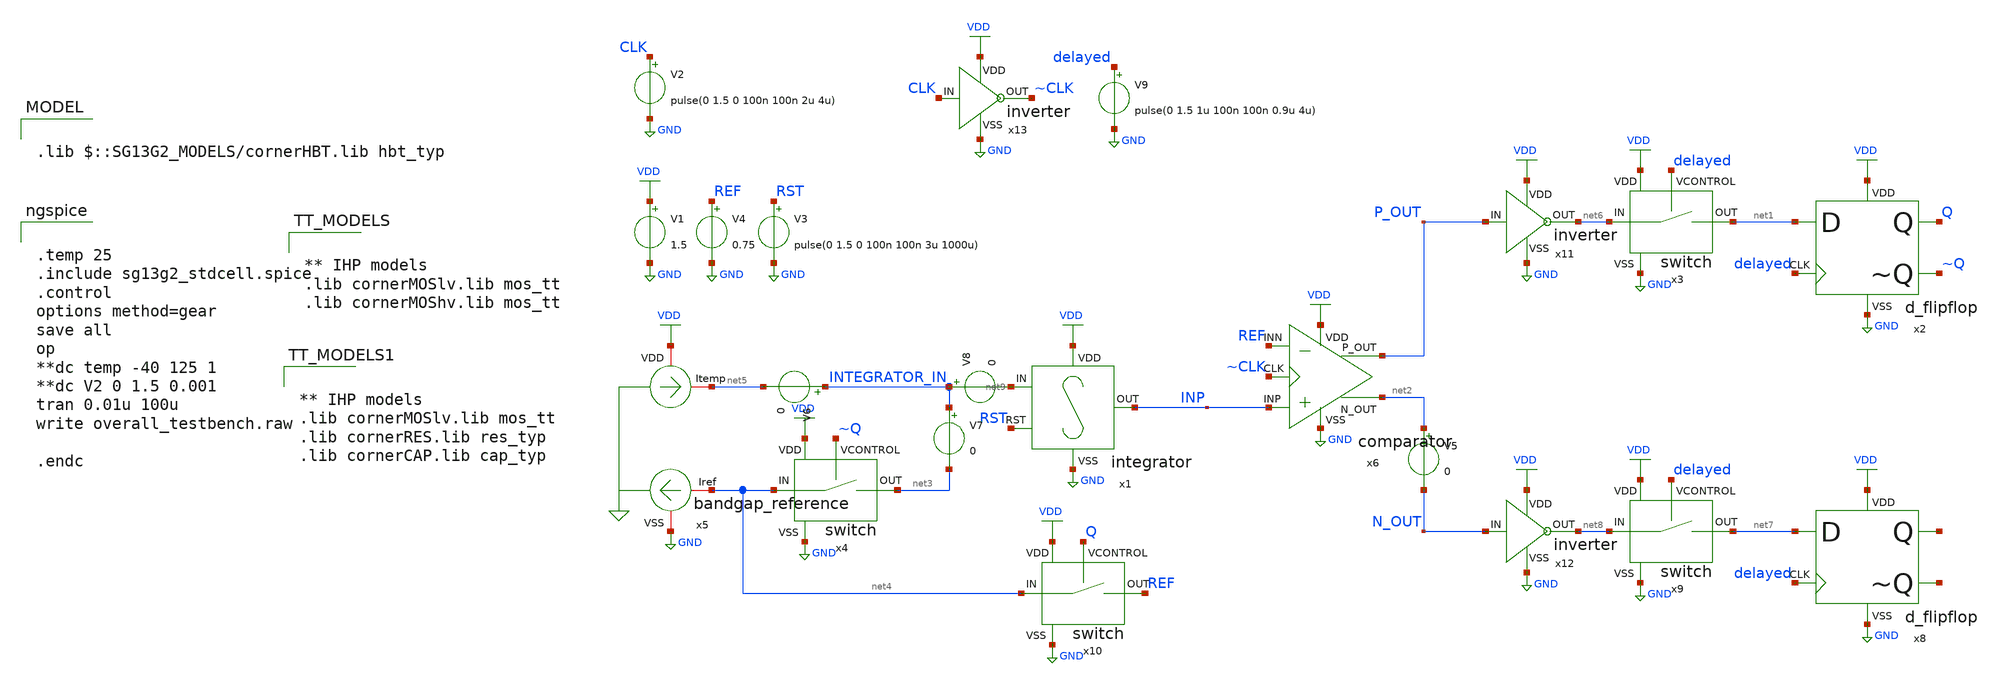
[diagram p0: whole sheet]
** sch_path: 10_xschem/overall_circuit_testbench.sch
**.subckt overall_circuit_testbench
x1 INP net9 VDD GND RST integrator
x4 net3 net4 VDD ~Q GND switch
V1 VDD GND 1.5
V3 RST GND pulse(0 1.5 0 100n 100n 3u 1000u)
x6 VDD P_OUT net2 ~CLK REF INP GND comparator
V4 REF GND 0.75
x2 Q ~Q net1 VDD GND delayed d_flipflop
x3 net1 net6 VDD delayed GND switch
x10 REF net4 VDD Q GND switch
V5 net2 N_OUT 0
V6 INTEGRATOR_IN net5 0
V7 INTEGRATOR_IN net3 0
x11 VDD P_OUT net6 GND inverter
x12 VDD N_OUT net8 GND inverter
x8 net10 net11 net7 VDD GND delayed d_flipflop
x9 net7 net8 VDD delayed GND switch
x13 VDD CLK ~CLK GND inverter
V2 CLK GND pulse(0 1.5 0 100n 100n 2u 4u)
V8 INTEGRATOR_IN net9 0
V9 delayed GND pulse(0 1.5 1u 100n 100n 0.9u 4u)
x5 VDD net5 net4 GND bandgap_reference
**** begin user architecture code


.temp 25
.include sg13g2_stdcell.spice
.control
options method=gear
save all
op
**dc temp -40 125 1
**dc V2 0 1.5 0.001
tran 0.01u 100u
write overall_testbench.raw

.endc




** IHP models
.lib cornerMOSlv.lib mos_tt
.lib cornerMOShv.lib mos_tt




** IHP models
.lib cornerMOSlv.lib mos_tt
.lib cornerRES.lib res_typ
.lib cornerCAP.lib cap_typ



.lib $::SG13G2_MODELS/cornerHBT.lib hbt_typ

**** end user architecture code
**.ends
.GLOBAL GND
.GLOBAL VDD
.end
